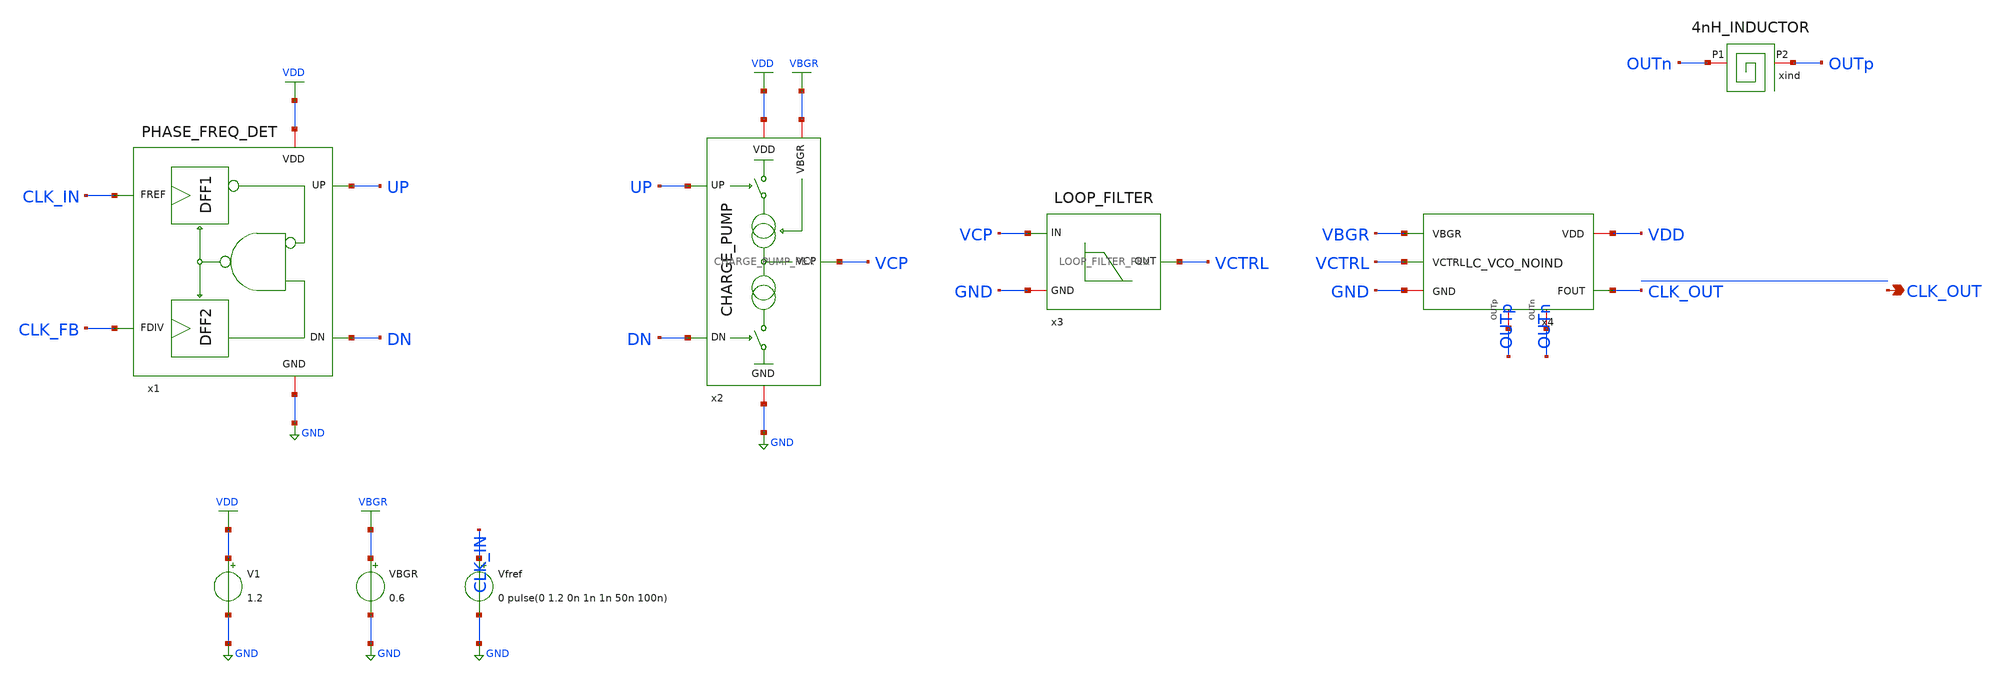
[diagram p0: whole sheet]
** sch_path: xschem/top-pll/tb_LC_VCO_FPLL_PEX.sch
**.subckt tb_LC_VCO_FPLL_PEX CLK_OUT
*.opin CLK_OUT
x1 CLK_IN UP VDD GND CLK_FB DN PHASE_FREQ_DET_PEX
x2 UP VDD VCP VBGR GND DN CHARGE_PUMP_PEX
x3 VCTRL VCP GND LOOP_FILTER_PEX
x4 OUTp OUTn CLK_OUT VCTRL VBGR GND VDD LC_VCO_NOIND
xind OUTn OUTp 4nH_INDUCTOR
V1 VDD GND 1.2
VBGR VBGR GND 0.6
Vfref CLK_IN GND 0 pulse(0 1.2 0n 1n 1n 50n 100n)
**** begin user architecture code



*****************************************************
* Closed-loop PLL testbench (post-layout, extracted blocks)
* VBGR is an ideal source: the bandgap is a test block, not part of the tapeout.
*****************************************************
.option temp=27
.param VDD=1.2
.option rshunt=1.0e12
.include 4nH_INDUCTOR.spice
.include ../simulations/stimuli_test.cir
* start-up kick: a noise-free run can stay at the unstable equilibrium at low VCTRL
.ic v(OUTp)=0.4
* extracted (Magic RC) netlists of the blocks; the inductor is the EM model above
.include ../pex/PHASE_FREQ_DET__PHASE_FREQ_DET/magic_RC/PHASE_FREQ_DET.pex.spice
.include ../pex/CHARGE_PUMP_V2__CHARGE_PUMP/magic_RC/CHARGE_PUMP.pex.spice
.include ../pex/LOOP_FILTER__LOOP_FILTER/magic_RC/LOOP_FILTER.pex.spice
.include ../pex/LC_VCO_NOIND__LC_VCO_NOIND/magic_RC/LC_VCO_NOIND.pex_sim.spice
* Divider: compiled behavioural model of the DSM + N-divider (dsm_and_freq_divider.so),
* verified separately at transistor level (tb_DSM_N_FREQ_DIV, tb_DSM_N_FREQ_DIV_PEX).
adut [ dn1 dn2 dn3 dn4 dn5 ] [ dn6 ] null dut
.model dut d_cosim simulation=../simulations/dsm_and_freq_divider.so
A1 [ CLK_OUT ] [ dn1 ] adc1
A2 [ rst ] [ dn2 ] adc1
A3 [ sclk ] [ dn3 ] adc1
A4 [ sdata ] [ dn4 ] adc1
A5 [ en ] [ dn5 ] adc1
* ADC threshold: 0.6 V = mid-swing of the extracted VCO output (measured -0.03 V to 1.22 V)
.model adc1 adc_bridge in_low=0.6 in_high=0.6
A6 [ dn6 ] [ CLK_FB ] dac1
.model dac1 dac_bridge out_low=0 out_high=1.2
* gear method is stable for long oscillator runs
.options reltol=1e-3 abstol=1e-9 vntol=1e-6 method=gear
.control
  * save only the low-frequency loop signals plus the output clock
  save v(vctrl) v(up) v(dn) v(clk_fb) v(clk_out) v(clk_in) v(vcp) v1#branch
  tran 10p 40u
  meas tran idd avg i(V1) from=20u to=40u
  remzerovec
  write tb_LC_VCO_FPLL_PEX_40u.raw v(vctrl) v(up) v(dn) v(clk_fb) v(clk_out) v(clk_in) v(vcp)
.endc






.lib cornerMOSlv.lib mos_tt
.lib cornerMOShv.lib mos_tt
.lib cornerHBT.lib hbt_typ
.lib cornerRES.lib res_typ
.lib cornerCAP.lib cap_typ
.include /foss/pdks/ihp-sg13g2/libs.ref/sg13g2_stdcell/spice/sg13g2_stdcell.spice
.global VDD GND



**** end user architecture code
**.ends
.GLOBAL VDD
.GLOBAL GND
.GLOBAL VBGR
.end
